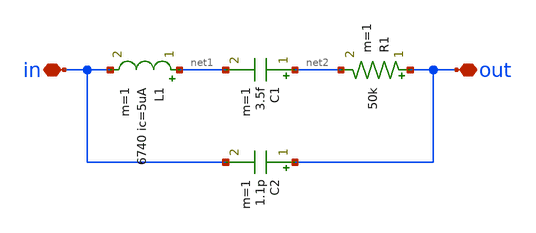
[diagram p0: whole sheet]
** sch_path: xschem/resonator_32k.sch
**.subckt resonator_32k out in
*.iopin out
*.iopin in
L1 net1 in 6740 ic=5uA m=1
C1 net2 net1 3.5f m=1
C2 out in 1.1p m=1
R1 out net2 50k m=1
**.ends
.end
